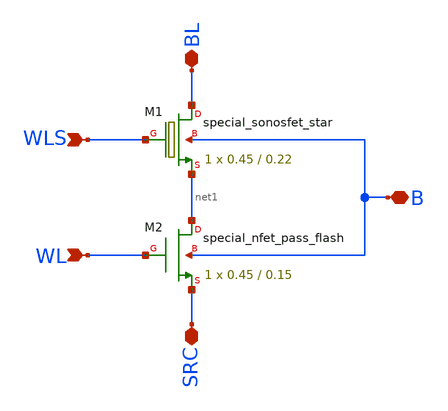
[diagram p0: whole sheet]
** sch_path: xschem/sonos_cell.sch
**.subckt sonos_cell WLS WL B BL SRC
*.ipin WLS
*.ipin WL
*.iopin B
*.iopin BL
*.iopin SRC
XM1 BL WLS net1 B sky130_fd_bs__special_sonosfet_star L=0.22 W=0.45 m=1
XM2 net1 WL SRC B sky130_fd_bs__special_nfet_pass_flash L=0.15 W=0.45 m=1
**.ends
.end
